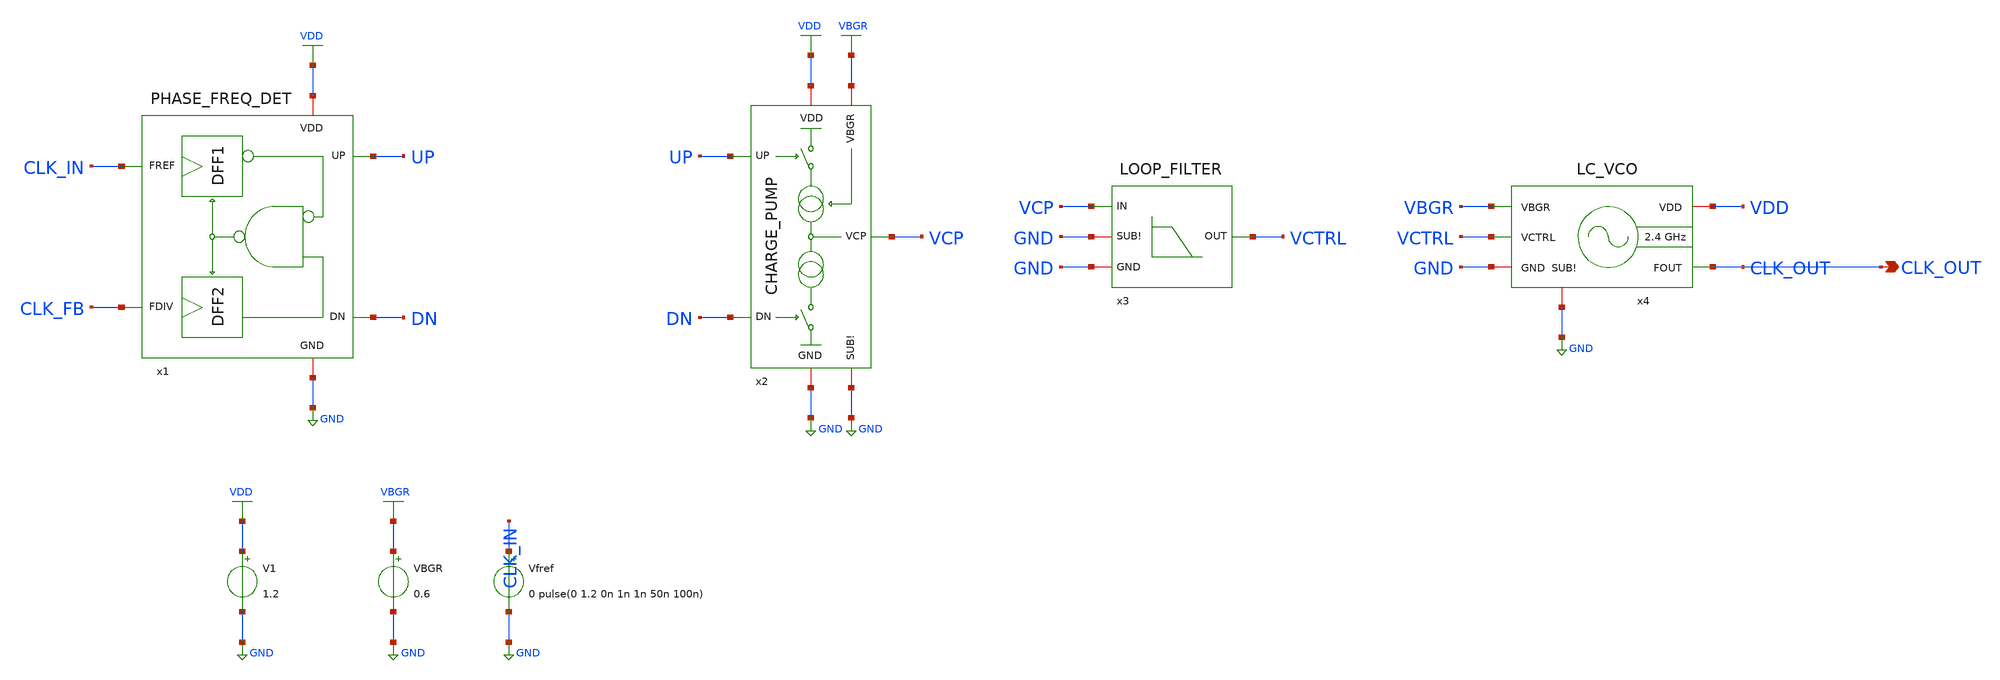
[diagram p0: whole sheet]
** sch_path: xschem/top-pll/tb_LC_VCO_FPLL.sch
**.subckt tb_LC_VCO_FPLL CLK_OUT
*.opin CLK_OUT
x1 CLK_IN UP VDD GND CLK_FB DN PHASE_FREQ_DET
x2 UP VDD VCP VBGR GND DN GND CHARGE_PUMP
x3 VCTRL VCP GND GND LOOP_FILTER
x4 VDD VCTRL GND CLK_OUT VBGR GND LC_VCO
V1 VDD GND 1.2
VBGR VBGR GND 0.6
Vfref CLK_IN GND 0 pulse(0 1.2 0n 1n 1n 50n 100n)
**** begin user architecture code



*****************************************************
* Closed-loop PLL testbench (pre-layout)
* VBGR is an ideal source: the bandgap is a test block, not part of the tapeout.
*****************************************************
.option temp=27
.param VDD=1.2
.option rshunt=1.0e12
.include 4nH_INDUCTOR.spice
.include ../simulations/stimuli_test.cir

* Divider: compiled behavioural model of the DSM + N-divider (dsm_and_freq_divider.so),
* verified separately at transistor level (tb_DSM_N_FREQ_DIV, tb_DSM_N_FREQ_DIV_PEX).
adut [ dn1 dn2 dn3 dn4 dn5 ] [ dn6 ] null dut
.model dut d_cosim simulation=../simulations/dsm_and_freq_divider.so
A1 [ CLK_OUT ] [ dn1 ] adc1
A2 [ rst ] [ dn2 ] adc1
A3 [ sclk ] [ dn3 ] adc1
A4 [ sdata ] [ dn4 ] adc1
A5 [ en ] [ dn5 ] adc1
* ADC threshold: value used in the paper deck
.model adc1 adc_bridge in_low=0.76 in_high=0.76
A6 [ dn6 ] [ CLK_FB ] dac1
.model dac1 dac_bridge out_low=0 out_high=1.2
* gear method is stable for long oscillator runs
.options reltol=1e-3 abstol=1e-9 vntol=1e-6 method=gear
.control
  * save only the low-frequency loop signals plus the output clock
  save v(vctrl) v(up) v(dn) v(clk_fb) v(clk_out) v(clk_in) v(vcp) v1#branch
  tran 10p 100u
  meas tran idd avg i(V1) from=60u to=100u
  remzerovec
  write tb_LC_VCO_FPLL_100u.raw v(vctrl) v(up) v(dn) v(clk_fb) v(clk_out) v(clk_in) v(vcp)
.endc






.lib cornerMOSlv.lib mos_tt
.lib cornerMOShv.lib mos_tt
.lib cornerHBT.lib hbt_typ
.lib cornerRES.lib res_typ
.lib cornerCAP.lib cap_typ
.include /foss/pdks/ihp-sg13g2/libs.ref/sg13g2_stdcell/spice/sg13g2_stdcell.spice
.global VDD GND



**** end user architecture code
**.ends
.GLOBAL VDD
.GLOBAL GND
.GLOBAL VBGR
.end
